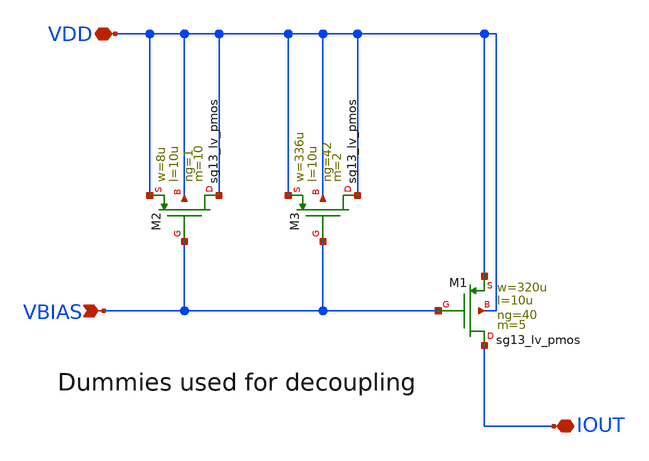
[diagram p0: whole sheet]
** sch_path: JKU_TC1/design_data/sfl-test-cells/xschem/tailsrcs/tail_src_p.sch
**.subckt tail_src_p VBIAS VDD IOUT
*.ipin VBIAS
*.iopin VDD
*.iopin IOUT
XM1 IOUT VBIAS VDD VDD sg13_lv_pmos w=320u l=10u ng=40 m=5 mm_ok=1
XM2 VDD VBIAS VDD VDD sg13_lv_pmos w=8u l=10u ng=1 m=10 mm_ok=1
XM3 VDD VBIAS VDD VDD sg13_lv_pmos w=336u l=10u ng=42 m=2 mm_ok=1
**.ends
.end
